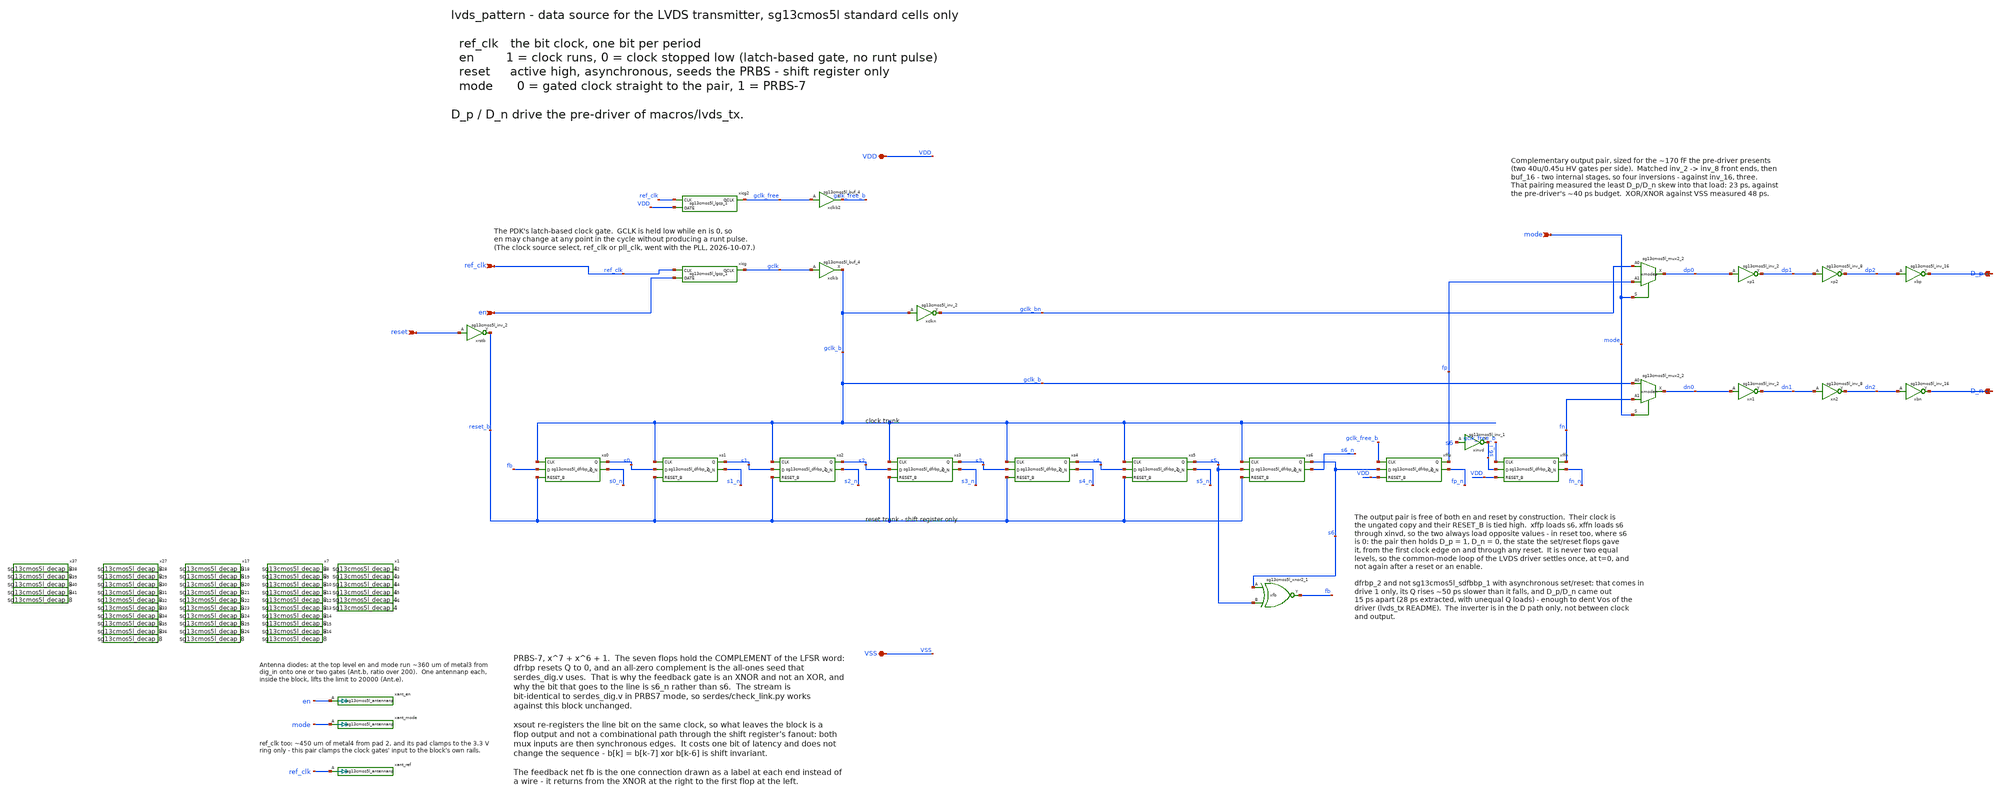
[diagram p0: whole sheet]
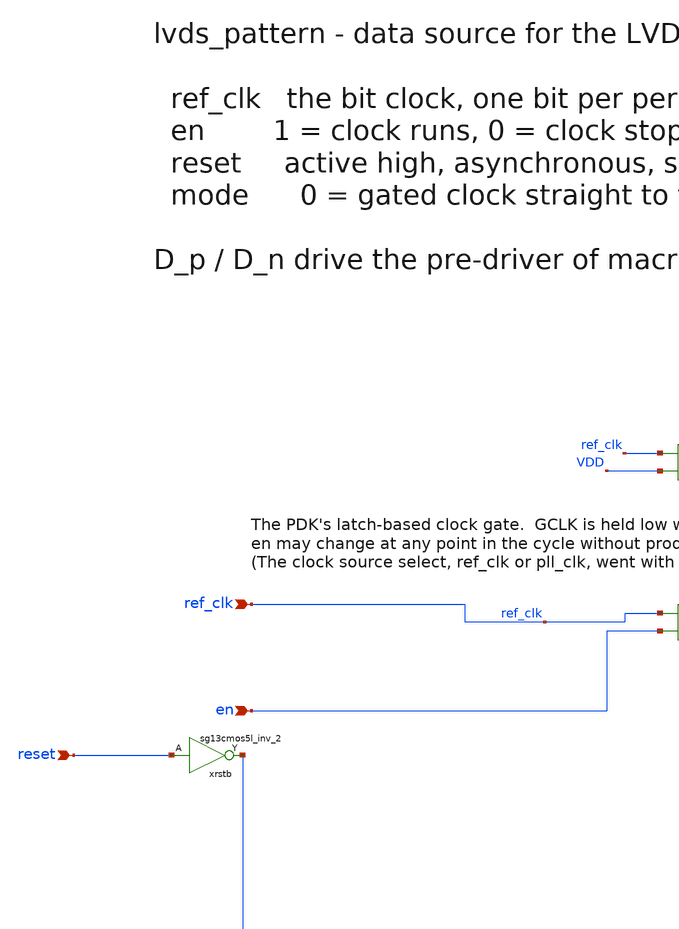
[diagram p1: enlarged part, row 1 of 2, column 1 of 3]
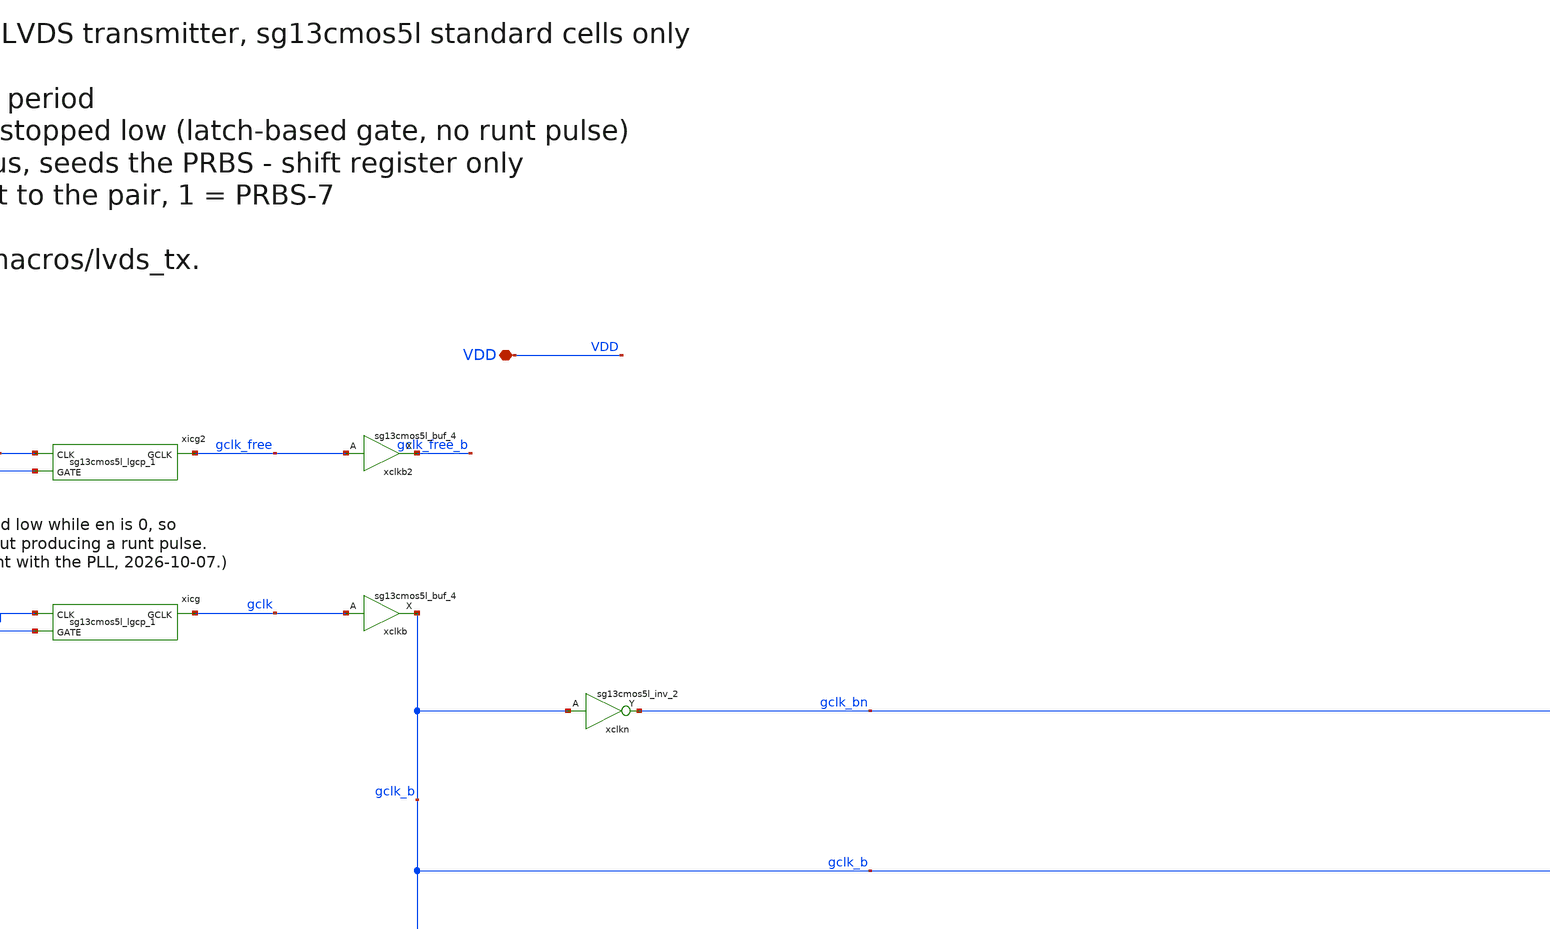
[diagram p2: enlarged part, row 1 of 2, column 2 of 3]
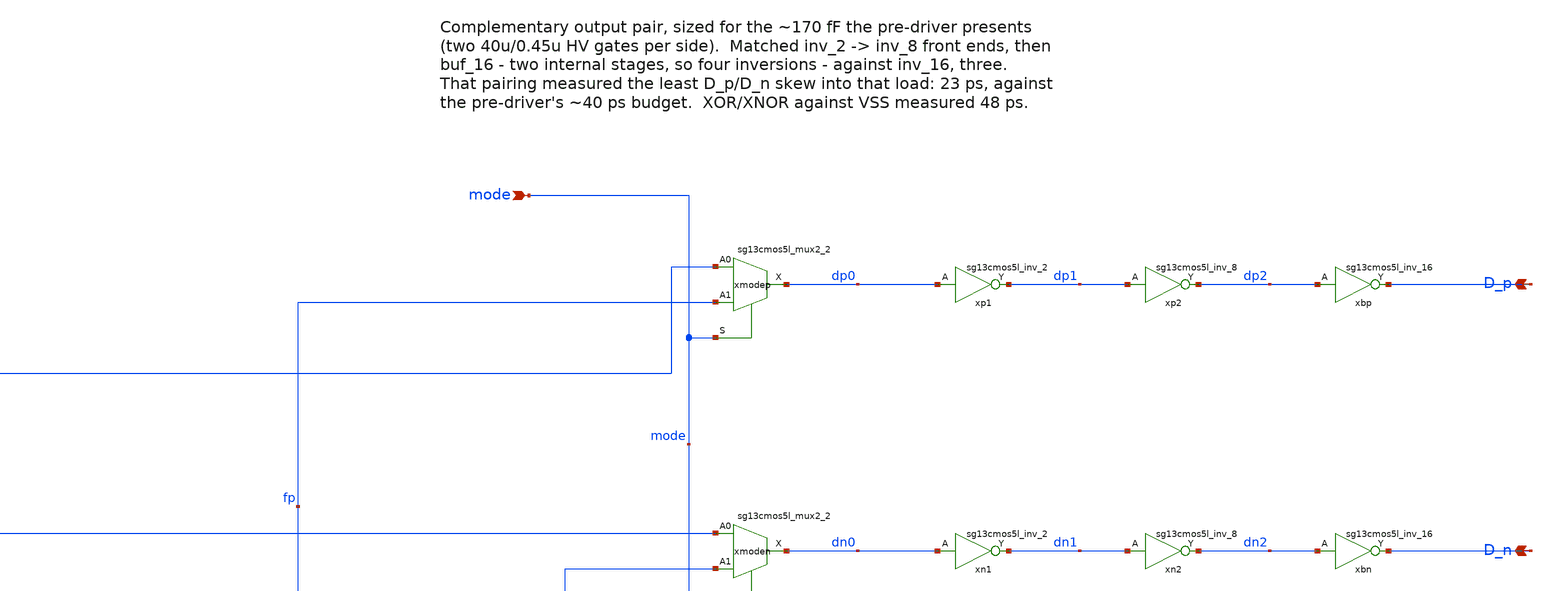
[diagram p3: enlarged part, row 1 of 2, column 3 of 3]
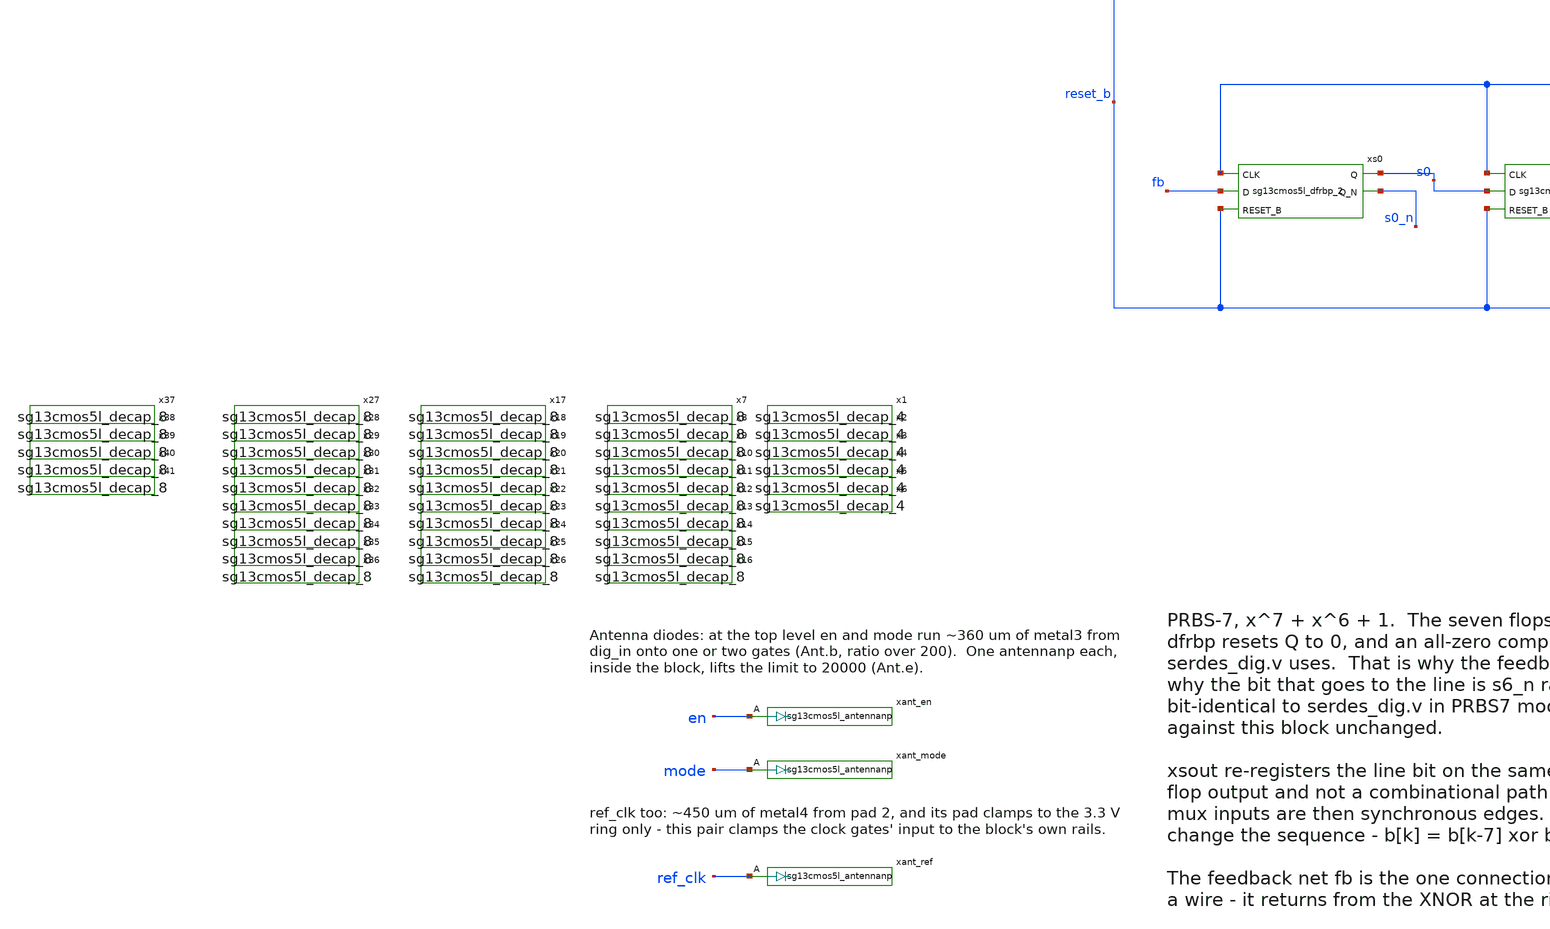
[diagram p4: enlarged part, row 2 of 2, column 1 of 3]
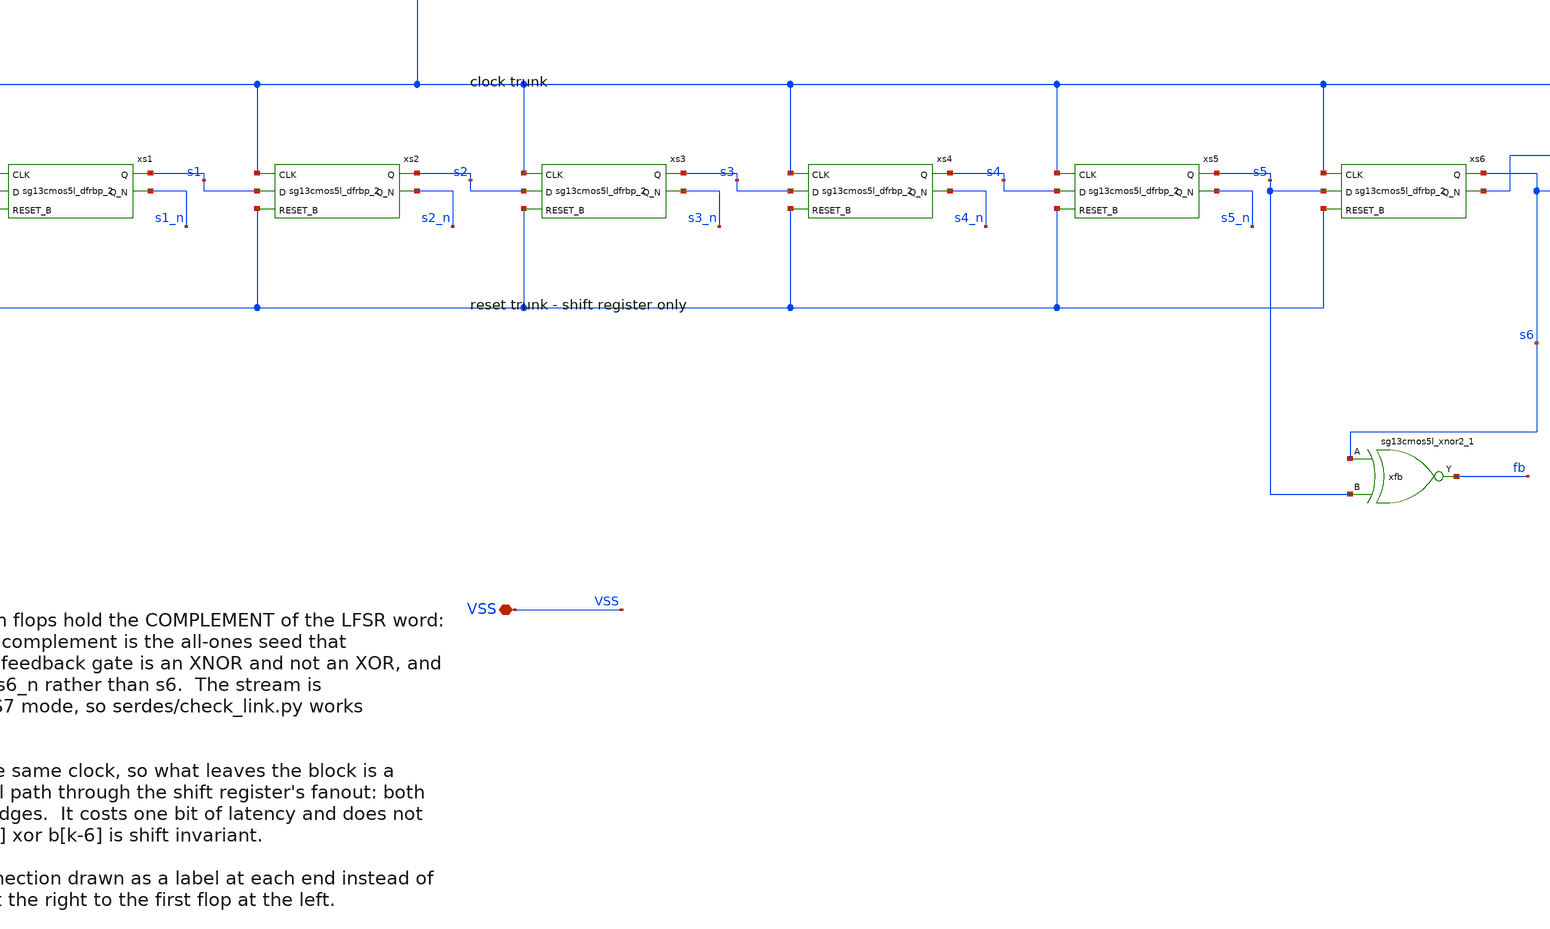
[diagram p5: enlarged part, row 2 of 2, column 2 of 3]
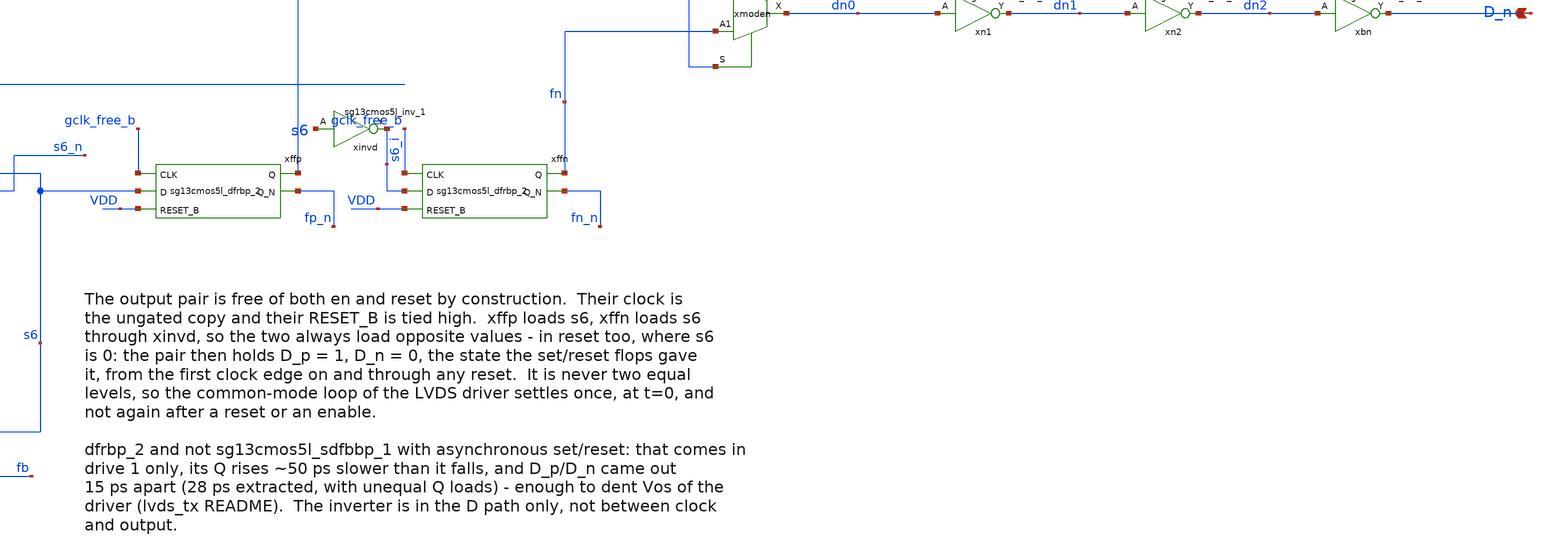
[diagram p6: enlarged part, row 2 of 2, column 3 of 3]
** sch_path: macros/lvds_pattern/schematic/xschem/lvds_pattern.sch
**.subckt lvds_pattern ref_clk en reset mode D_p D_n VDD VSS
*.ipin ref_clk
*.ipin en
*.ipin reset
*.ipin mode
*.opin D_p
*.opin D_n
*.iopin VDD
*.iopin VSS
xicg gclk ref_clk en VDD VSS sg13cmos5l_lgcp_1
xclkb gclk_b gclk VDD VSS sg13cmos5l_buf_4
xicg2 gclk_free ref_clk VDD VDD VSS sg13cmos5l_lgcp_1
xclkb2 gclk_free_b gclk_free VDD VSS sg13cmos5l_buf_4
xrstb reset_b reset VDD VSS sg13cmos5l_inv_2
xs0 s0 s0_n gclk_b fb reset_b VDD VSS sg13cmos5l_dfrbp_2
xs1 s1 s1_n gclk_b s0 reset_b VDD VSS sg13cmos5l_dfrbp_2
xs2 s2 s2_n gclk_b s1 reset_b VDD VSS sg13cmos5l_dfrbp_2
xs3 s3 s3_n gclk_b s2 reset_b VDD VSS sg13cmos5l_dfrbp_2
xs4 s4 s4_n gclk_b s3 reset_b VDD VSS sg13cmos5l_dfrbp_2
xs5 s5 s5_n gclk_b s4 reset_b VDD VSS sg13cmos5l_dfrbp_2
xs6 s6 s6_n gclk_b s5 reset_b VDD VSS sg13cmos5l_dfrbp_2
xfb fb s6 s5 VDD VSS sg13cmos5l_xnor2_1
xclkn gclk_bn gclk_b VDD VSS sg13cmos5l_inv_2
xmodep dp0 gclk_bn fp mode VDD VSS sg13cmos5l_mux2_2
xmoden dn0 gclk_b fn mode VDD VSS sg13cmos5l_mux2_2
xp1 dp1 dp0 VDD VSS sg13cmos5l_inv_2
xp2 dp2 dp1 VDD VSS sg13cmos5l_inv_8
xbp D_p dp2 VDD VSS sg13cmos5l_inv_16
xn1 dn1 dn0 VDD VSS sg13cmos5l_inv_2
xn2 dn2 dn1 VDD VSS sg13cmos5l_inv_8
xbn D_n dn2 VDD VSS sg13cmos5l_inv_16
xffn fn fn_n gclk_free_b s6_i VDD VDD VSS sg13cmos5l_dfrbp_2
xffp fp fp_n gclk_free_b s6 VDD VDD VSS sg13cmos5l_dfrbp_2
x1 VDD VSS sg13cmos5l_decap_4
x2 VDD VSS sg13cmos5l_decap_4
x3 VDD VSS sg13cmos5l_decap_4
x4 VDD VSS sg13cmos5l_decap_4
x5 VDD VSS sg13cmos5l_decap_4
x6 VDD VSS sg13cmos5l_decap_4
x7 VDD VSS sg13cmos5l_decap_8
x8 VDD VSS sg13cmos5l_decap_8
x9 VDD VSS sg13cmos5l_decap_8
x10 VDD VSS sg13cmos5l_decap_8
x11 VDD VSS sg13cmos5l_decap_8
x12 VDD VSS sg13cmos5l_decap_8
x13 VDD VSS sg13cmos5l_decap_8
x14 VDD VSS sg13cmos5l_decap_8
x15 VDD VSS sg13cmos5l_decap_8
x16 VDD VSS sg13cmos5l_decap_8
x17 VDD VSS sg13cmos5l_decap_8
x18 VDD VSS sg13cmos5l_decap_8
x19 VDD VSS sg13cmos5l_decap_8
x20 VDD VSS sg13cmos5l_decap_8
x21 VDD VSS sg13cmos5l_decap_8
x22 VDD VSS sg13cmos5l_decap_8
x23 VDD VSS sg13cmos5l_decap_8
x24 VDD VSS sg13cmos5l_decap_8
x25 VDD VSS sg13cmos5l_decap_8
x26 VDD VSS sg13cmos5l_decap_8
x27 VDD VSS sg13cmos5l_decap_8
x28 VDD VSS sg13cmos5l_decap_8
x29 VDD VSS sg13cmos5l_decap_8
x30 VDD VSS sg13cmos5l_decap_8
x31 VDD VSS sg13cmos5l_decap_8
x32 VDD VSS sg13cmos5l_decap_8
x33 VDD VSS sg13cmos5l_decap_8
x34 VDD VSS sg13cmos5l_decap_8
x35 VDD VSS sg13cmos5l_decap_8
x36 VDD VSS sg13cmos5l_decap_8
x37 VDD VSS sg13cmos5l_decap_8
x38 VDD VSS sg13cmos5l_decap_8
x39 VDD VSS sg13cmos5l_decap_8
x40 VDD VSS sg13cmos5l_decap_8
x41 VDD VSS sg13cmos5l_decap_8
xinvd s6_i s6 VDD VSS sg13cmos5l_inv_1
xant_en en VDD VSS sg13cmos5l_antennanp
xant_mode mode VDD VSS sg13cmos5l_antennanp
xant_ref ref_clk VDD VSS sg13cmos5l_antennanp
**.ends
.end
